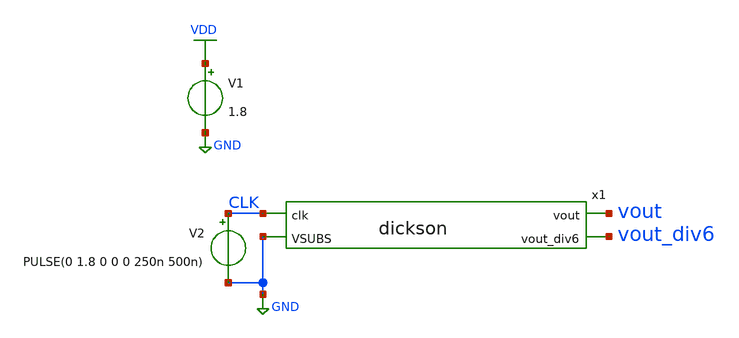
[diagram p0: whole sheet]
** sch_path: xschem/testbench.sch
**.subckt testbench
x1 vout CLK GND vout_div6 dickson
V1 VDD GND 1.8
V2 CLK GND PULSE(0 1.8 0 0 0 250n 500n)
**** begin user architecture code

** opencircuitdesign pdks install
.lib $::SKYWATER_MODELS/sky130.lib.spice tt





.tran 10n 100u
.save all

.control
run
write testbench.raw
.endc


**** end user architecture code
**.ends
.GLOBAL GND
.GLOBAL VDD
.end
